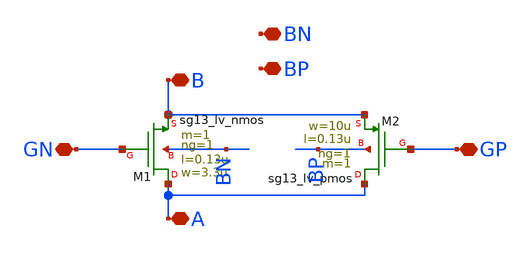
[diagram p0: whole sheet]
** sch_path: Day2/transmission_gate.sch
**.subckt transmission_gate B GN A GP BN BP
*.iopin B
*.iopin GN
*.iopin A
*.iopin GP
*.iopin BN
*.iopin BP
XM1 A GN B BN sg13_lv_nmos w=3.3u l=0.13u ng=1 m=1 mm_ok=1
XM2 A GP B BP sg13_lv_pmos w=10u l=0.13u ng=1 m=1 mm_ok=1
**.ends
.end
